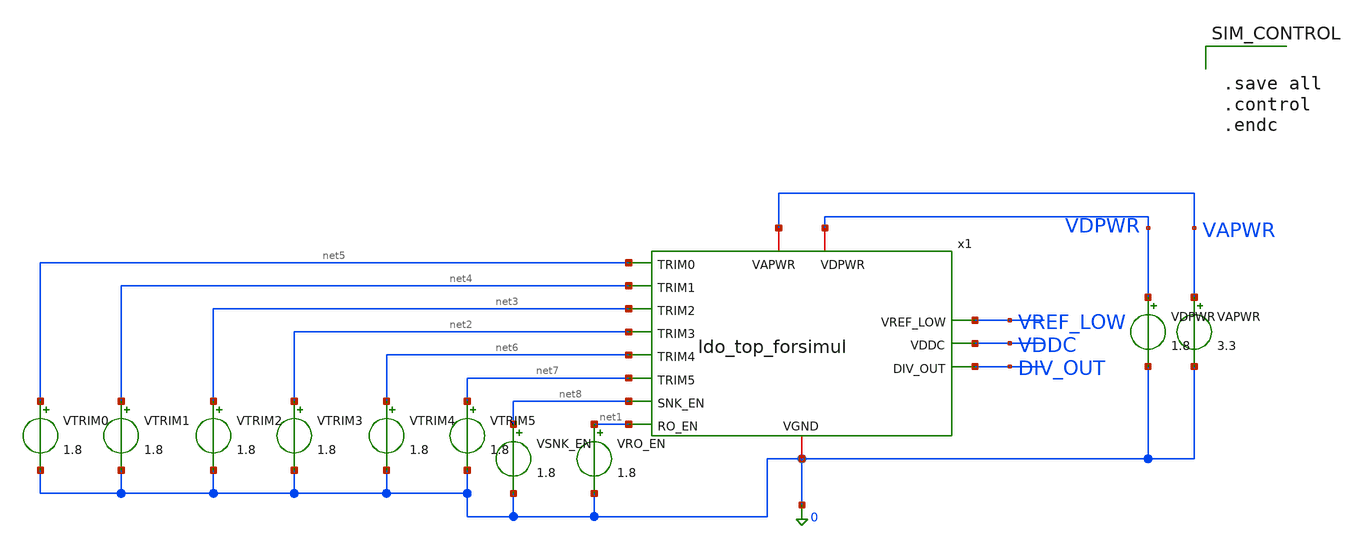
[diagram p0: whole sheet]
** sch_path: designs/bgr_ldo/ldo/ldo_top_tb.sch
**.subckt ldo_top_tb
VAPWR VAPWR 0 3.3
VDPWR VDPWR 0 1.8
VRO_EN net1 0 1.8
VSNK_EN net8 0 1.8
VTRIM3 net2 0 1.8
VTRIM2 net3 0 1.8
VTRIM1 net4 0 1.8
VTRIM0 net5 0 1.8
x1 net5 VAPWR net4 VREF_LOW VDDC net8 net3 0 VDPWR net2 DIV_OUT net1 net7 net6 ldo_top_forsimul
VTRIM4 net6 0 1.8
VTRIM5 net7 0 1.8
**** begin user architecture code

** opencircuitdesign pdks install
.lib $::SKYWATER_MODELS/sky130.lib.spice tt



.save all
.control
.endc

**** end user architecture code
**.ends
.end
